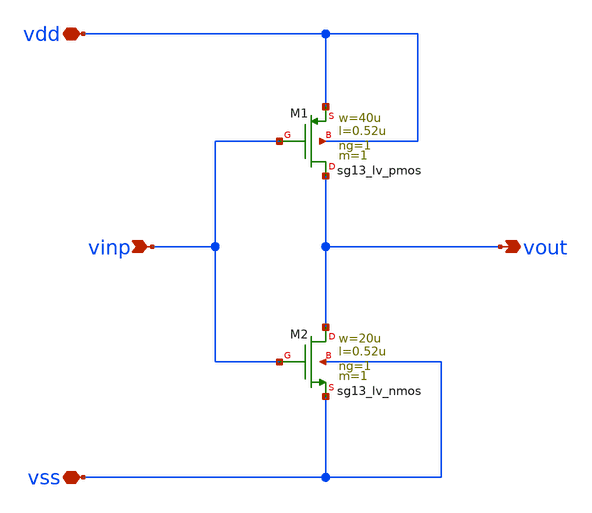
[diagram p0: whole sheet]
** sch_path: Schematics/Analog_Inverter.sch
**.subckt Analog_Inverter vinp vdd vss vout
*.ipin vinp
*.iopin vdd
*.iopin vss
*.opin vout
XM1 vout vinp vdd vdd sg13_lv_pmos w=40u l=0.52u ng=1 m=1 mm_ok=1
XM2 vout vinp vss vss sg13_lv_nmos w=20u l=0.52u ng=1 m=1 mm_ok=1
**.ends
.end
